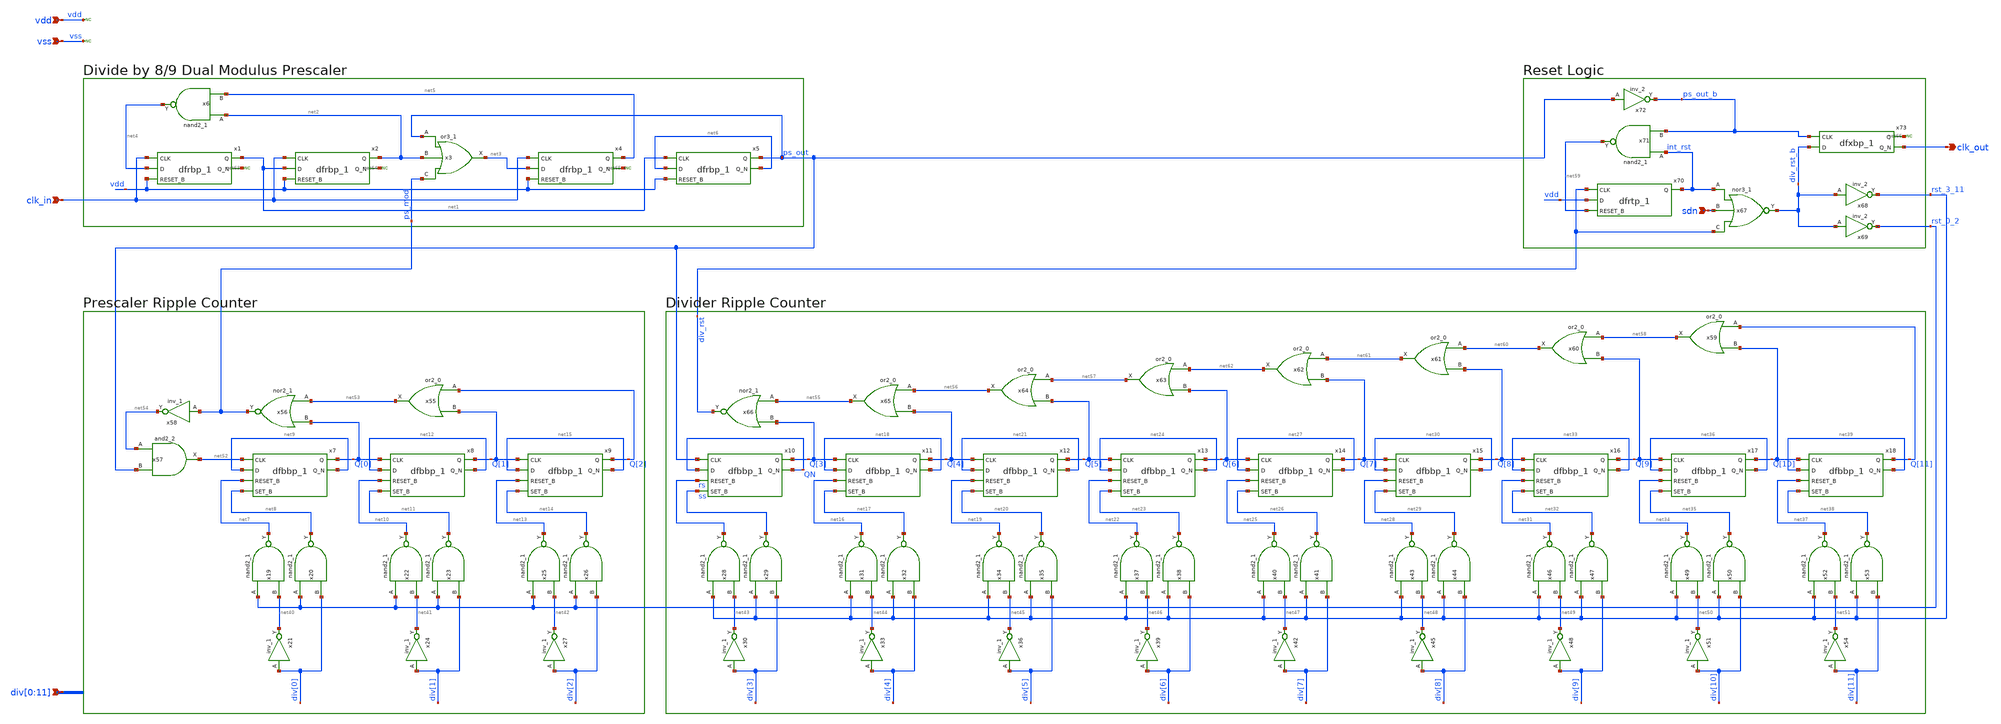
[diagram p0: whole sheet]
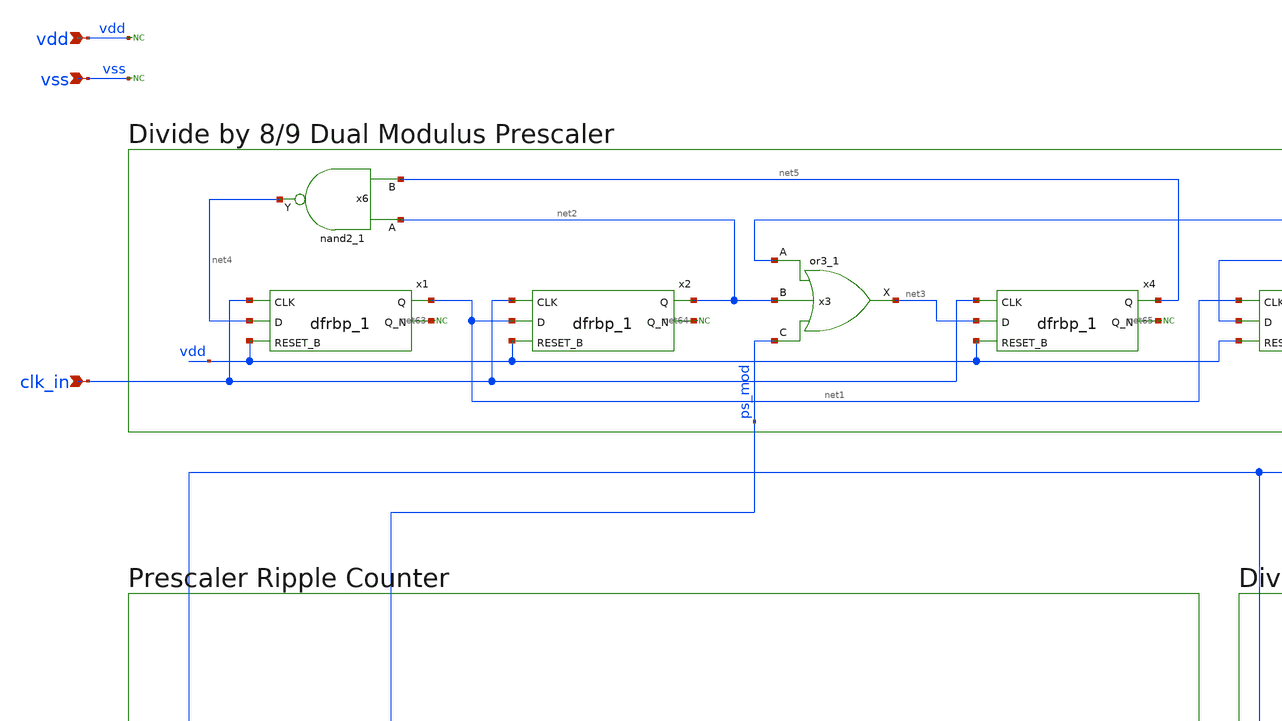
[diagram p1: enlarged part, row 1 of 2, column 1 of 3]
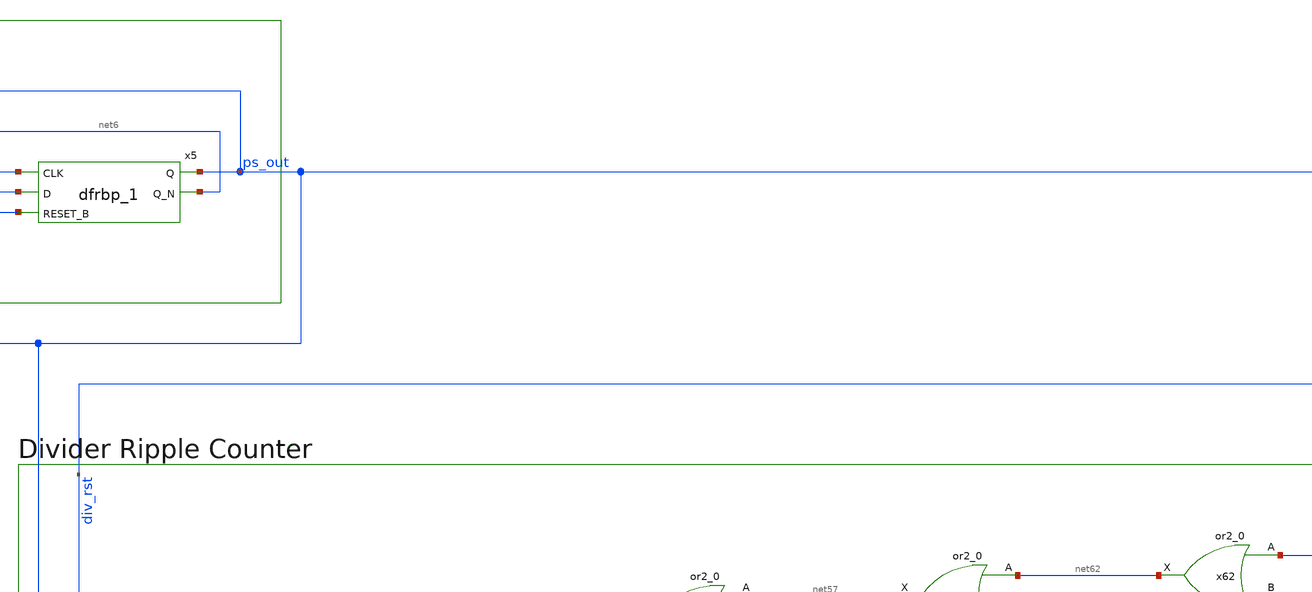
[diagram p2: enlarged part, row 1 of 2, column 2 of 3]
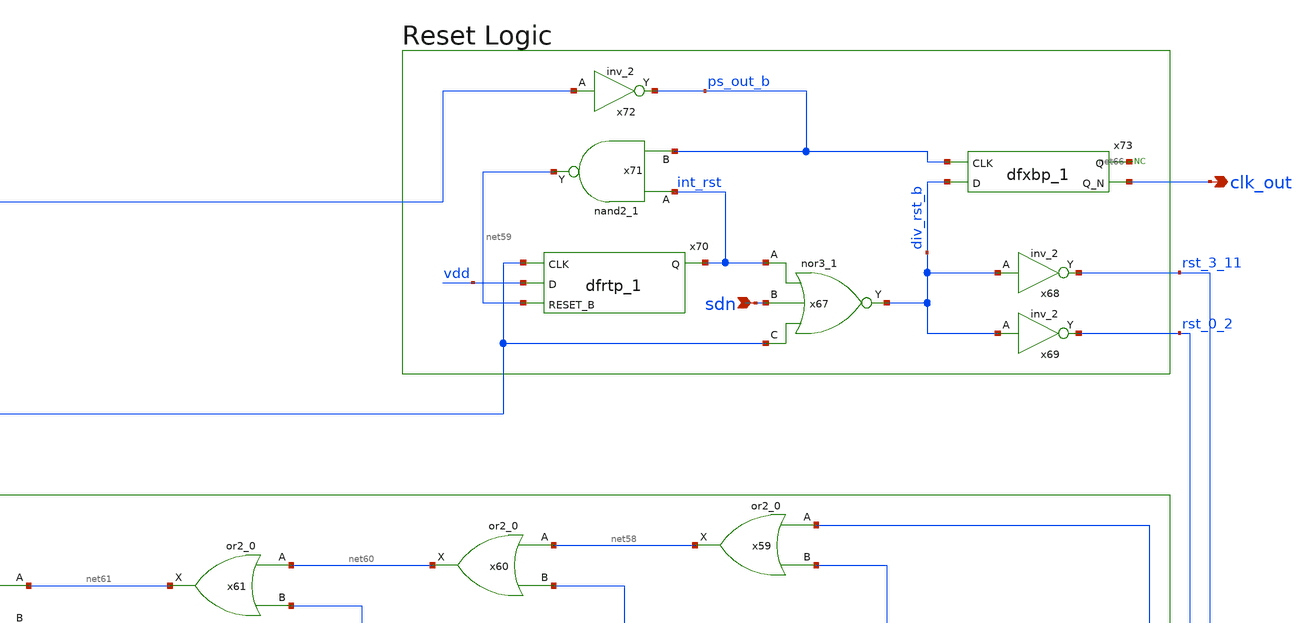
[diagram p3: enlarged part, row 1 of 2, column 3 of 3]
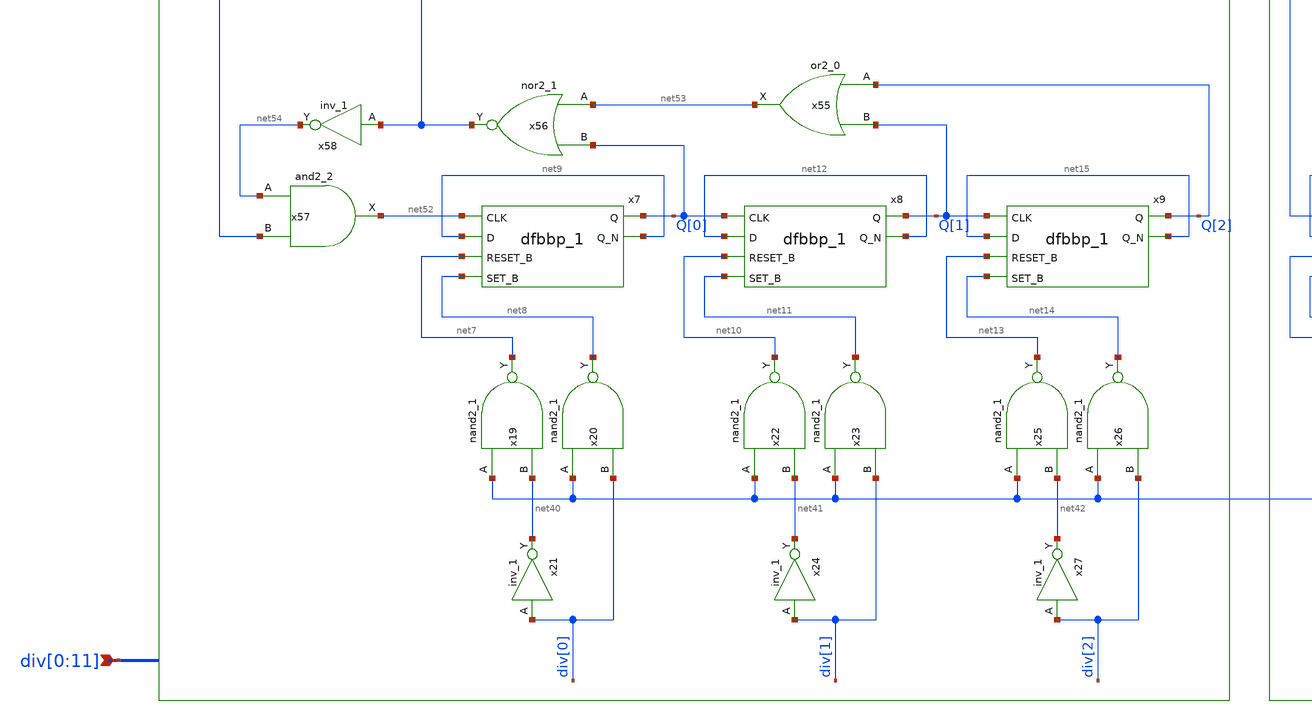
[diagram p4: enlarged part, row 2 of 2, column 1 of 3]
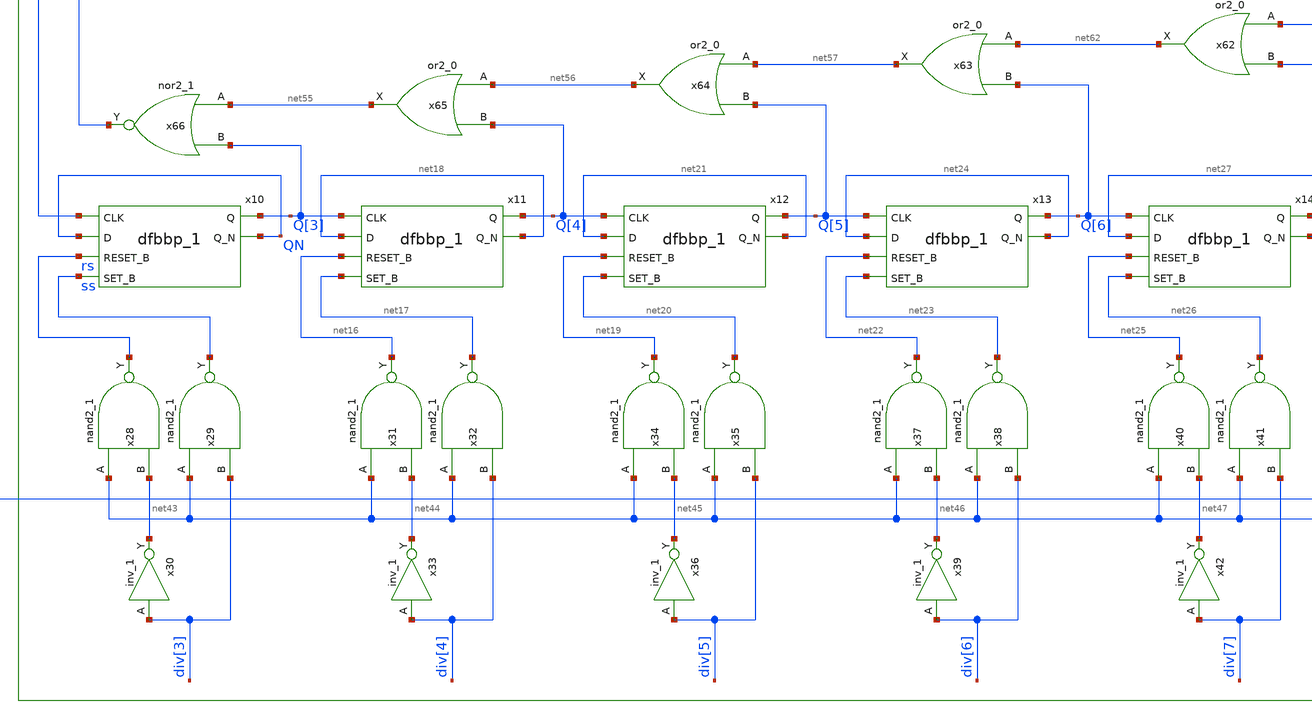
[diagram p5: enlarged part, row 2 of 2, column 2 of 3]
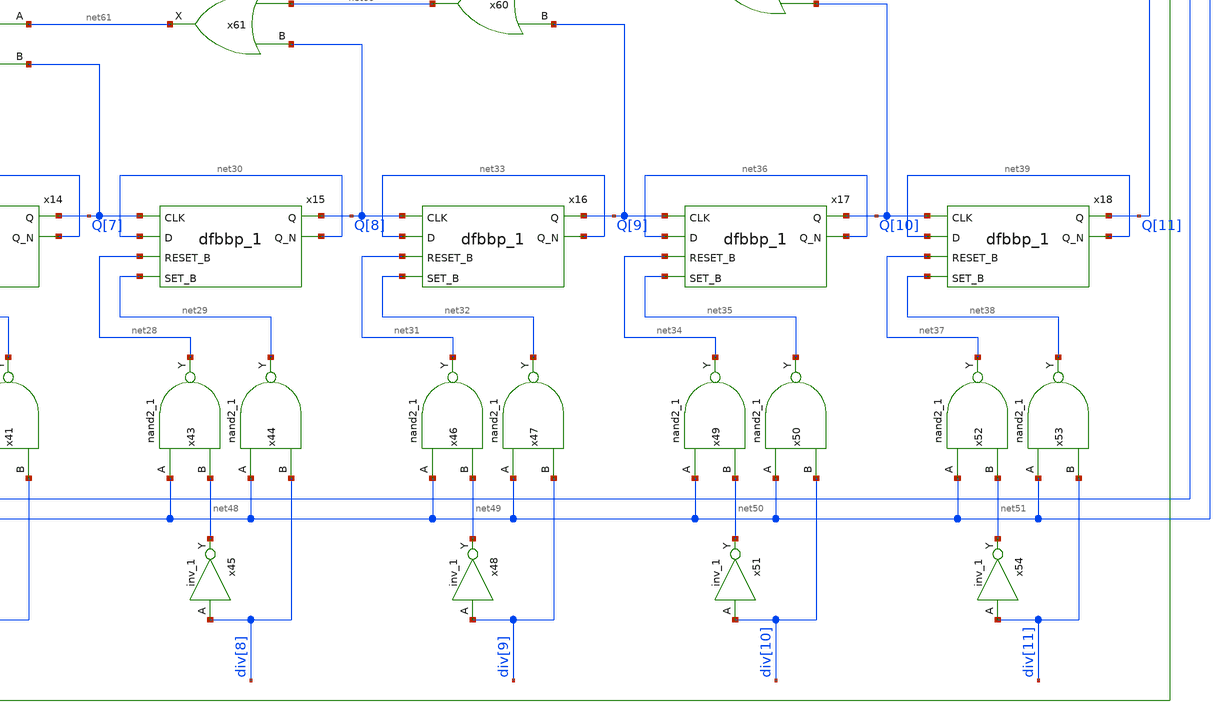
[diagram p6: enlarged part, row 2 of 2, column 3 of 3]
** sch_path: pll/pll_divider/xschem/pll_divider.sch
**.subckt pll_divider clk_in
*+ div[0],div[1],div[2],div[3],div[4],div[5],div[6],div[7],div[8],div[9],div[10],div[11] sdn clk_out vss vdd
*.ipin clk_in
*.ipin div[0],div[1],div[2],div[3],div[4],div[5],div[6],div[7],div[8],div[9],div[10],div[11]
*.ipin sdn
*.opin clk_out
*.ipin vss
*.ipin vdd
x1 clk_in net4 vdd vss vss vdd vdd net1 net63 sky130_fd_sc_hd__dfrbp_1
x2 clk_in net1 vdd vss vss vdd vdd net2 net64 sky130_fd_sc_hd__dfrbp_1
x4 clk_in net3 vdd vss vss vdd vdd net5 net65 sky130_fd_sc_hd__dfrbp_1
x5 net1 net6 vdd vss vss vdd vdd ps_out net6 sky130_fd_sc_hd__dfrbp_1
x3 ps_out net2 ps_mod vss vss vdd vdd net3 sky130_fd_sc_hd__or3_1
x6 net2 net5 vss vss vdd vdd net4 sky130_fd_sc_hd__nand2_1
x7 net52 net9 net7 net8 vss vss vdd vdd Q[0] net9 sky130_fd_sc_hd__dfbbp_1
x8 Q[0] net12 net10 net11 vss vss vdd vdd Q[1] net12 sky130_fd_sc_hd__dfbbp_1
x9 Q[1] net15 net13 net14 vss vss vdd vdd Q[2] net15 sky130_fd_sc_hd__dfbbp_1
x10 ps_out QN rs ss vss vss vdd vdd Q[3] QN sky130_fd_sc_hd__dfbbp_1
x11 Q[3] net18 net16 net17 vss vss vdd vdd Q[4] net18 sky130_fd_sc_hd__dfbbp_1
x12 Q[4] net21 net19 net20 vss vss vdd vdd Q[5] net21 sky130_fd_sc_hd__dfbbp_1
x13 Q[5] net24 net22 net23 vss vss vdd vdd Q[6] net24 sky130_fd_sc_hd__dfbbp_1
x14 Q[6] net27 net25 net26 vss vss vdd vdd Q[7] net27 sky130_fd_sc_hd__dfbbp_1
x15 Q[7] net30 net28 net29 vss vss vdd vdd Q[8] net30 sky130_fd_sc_hd__dfbbp_1
x16 Q[8] net33 net31 net32 vss vss vdd vdd Q[9] net33 sky130_fd_sc_hd__dfbbp_1
x17 Q[9] net36 net34 net35 vss vss vdd vdd Q[10] net36 sky130_fd_sc_hd__dfbbp_1
x18 Q[10] net39 net37 net38 vss vss vdd vdd Q[11] net39 sky130_fd_sc_hd__dfbbp_1
x19 rst_0_2 net40 vss vss vdd vdd net7 sky130_fd_sc_hd__nand2_1
x20 rst_0_2 div[0] vss vss vdd vdd net8 sky130_fd_sc_hd__nand2_1
x21 div[0] vss vss vdd vdd net40 sky130_fd_sc_hd__inv_1
x22 rst_0_2 net41 vss vss vdd vdd net10 sky130_fd_sc_hd__nand2_1
x23 rst_0_2 div[1] vss vss vdd vdd net11 sky130_fd_sc_hd__nand2_1
x24 div[1] vss vss vdd vdd net41 sky130_fd_sc_hd__inv_1
x25 rst_0_2 net42 vss vss vdd vdd net13 sky130_fd_sc_hd__nand2_1
x26 rst_0_2 div[2] vss vss vdd vdd net14 sky130_fd_sc_hd__nand2_1
x27 div[2] vss vss vdd vdd net42 sky130_fd_sc_hd__inv_1
x28 rst_3_11 net43 vss vss vdd vdd rs sky130_fd_sc_hd__nand2_1
x29 rst_3_11 div[3] vss vss vdd vdd ss sky130_fd_sc_hd__nand2_1
x30 div[3] vss vss vdd vdd net43 sky130_fd_sc_hd__inv_1
x31 rst_3_11 net44 vss vss vdd vdd net16 sky130_fd_sc_hd__nand2_1
x32 rst_3_11 div[4] vss vss vdd vdd net17 sky130_fd_sc_hd__nand2_1
x33 div[4] vss vss vdd vdd net44 sky130_fd_sc_hd__inv_1
x34 rst_3_11 net45 vss vss vdd vdd net19 sky130_fd_sc_hd__nand2_1
x35 rst_3_11 div[5] vss vss vdd vdd net20 sky130_fd_sc_hd__nand2_1
x36 div[5] vss vss vdd vdd net45 sky130_fd_sc_hd__inv_1
x37 rst_3_11 net46 vss vss vdd vdd net22 sky130_fd_sc_hd__nand2_1
x38 rst_3_11 div[6] vss vss vdd vdd net23 sky130_fd_sc_hd__nand2_1
x39 div[6] vss vss vdd vdd net46 sky130_fd_sc_hd__inv_1
x40 rst_3_11 net47 vss vss vdd vdd net25 sky130_fd_sc_hd__nand2_1
x41 rst_3_11 div[7] vss vss vdd vdd net26 sky130_fd_sc_hd__nand2_1
x42 div[7] vss vss vdd vdd net47 sky130_fd_sc_hd__inv_1
x43 rst_3_11 net48 vss vss vdd vdd net28 sky130_fd_sc_hd__nand2_1
x44 rst_3_11 div[8] vss vss vdd vdd net29 sky130_fd_sc_hd__nand2_1
x45 div[8] vss vss vdd vdd net48 sky130_fd_sc_hd__inv_1
x46 rst_3_11 net49 vss vss vdd vdd net31 sky130_fd_sc_hd__nand2_1
x47 rst_3_11 div[9] vss vss vdd vdd net32 sky130_fd_sc_hd__nand2_1
x48 div[9] vss vss vdd vdd net49 sky130_fd_sc_hd__inv_1
x49 rst_3_11 net50 vss vss vdd vdd net34 sky130_fd_sc_hd__nand2_1
x50 rst_3_11 div[10] vss vss vdd vdd net35 sky130_fd_sc_hd__nand2_1
x51 div[10] vss vss vdd vdd net50 sky130_fd_sc_hd__inv_1
x52 rst_3_11 net51 vss vss vdd vdd net37 sky130_fd_sc_hd__nand2_1
x53 rst_3_11 div[11] vss vss vdd vdd net38 sky130_fd_sc_hd__nand2_1
x54 div[11] vss vss vdd vdd net51 sky130_fd_sc_hd__inv_1
x55 Q[2] Q[1] vss vss vdd vdd net53 sky130_fd_sc_hd__or2_0
x56 net53 Q[0] vss vss vdd vdd ps_mod sky130_fd_sc_hd__nor2_1
x58 ps_mod vss vss vdd vdd net54 sky130_fd_sc_hd__inv_1
x59 Q[11] Q[10] vss vss vdd vdd net58 sky130_fd_sc_hd__or2_0
x60 net58 Q[9] vss vss vdd vdd net60 sky130_fd_sc_hd__or2_0
x61 net60 Q[8] vss vss vdd vdd net61 sky130_fd_sc_hd__or2_0
x62 net61 Q[7] vss vss vdd vdd net62 sky130_fd_sc_hd__or2_0
x63 net62 Q[6] vss vss vdd vdd net57 sky130_fd_sc_hd__or2_0
x64 net57 Q[5] vss vss vdd vdd net56 sky130_fd_sc_hd__or2_0
x65 net56 Q[4] vss vss vdd vdd net55 sky130_fd_sc_hd__or2_0
x66 net55 Q[3] vss vss vdd vdd div_rst sky130_fd_sc_hd__nor2_1
x67 int_rst sdn div_rst vss vss vdd vdd div_rst_b sky130_fd_sc_hd__nor3_1
x68 div_rst_b vss vss vdd vdd rst_3_11 sky130_fd_sc_hd__inv_2
x69 div_rst_b vss vss vdd vdd rst_0_2 sky130_fd_sc_hd__inv_2
x70 div_rst vdd net59 vss vss vdd vdd int_rst sky130_fd_sc_hd__dfrtp_1
x71 int_rst ps_out_b vss vss vdd vdd net59 sky130_fd_sc_hd__nand2_1
x73 ps_out_b div_rst_b vss vss vdd vdd net66 clk_out sky130_fd_sc_hd__dfxbp_1
x72 ps_out vss vss vdd vdd ps_out_b sky130_fd_sc_hd__inv_2
x57 net54 ps_out vss vss vdd vdd net52 sky130_fd_sc_hd__and2_2
* noconn vss
* noconn vdd
* noconn #net65
* noconn #net64
* noconn #net63
* noconn #net66
**** begin user architecture code

.options wnflag=1
.include $::SKYWATER_MODELS/cells/nfet_01v8/sky130_fd_pr__nfet_01v8__tt.corner.spice
.include $::SKYWATER_MODELS/cells/nfet_01v8_lvt/sky130_fd_pr__nfet_01v8_lvt__tt.corner.spice
.include $::SKYWATER_MODELS/cells/pfet_01v8/sky130_fd_pr__pfet_01v8__tt.corner.spice
.include $::SKYWATER_MODELS/cells/nfet_03v3_nvt/sky130_fd_pr__nfet_03v3_nvt__tt.corner.spice
.include $::SKYWATER_MODELS/cells/nfet_05v0_nvt/sky130_fd_pr__nfet_05v0_nvt__tt.corner.spice
.include $::SKYWATER_MODELS/cells/esd_nfet_01v8/sky130_fd_pr__esd_nfet_01v8__tt.corner.spice
.include $::SKYWATER_MODELS/cells/pfet_01v8_lvt/sky130_fd_pr__pfet_01v8_lvt__tt.corner.spice
.include $::SKYWATER_MODELS/cells/pfet_01v8_hvt/sky130_fd_pr__pfet_01v8_hvt__tt.corner.spice
.include $::SKYWATER_MODELS/cells/esd_pfet_g5v0d10v5/sky130_fd_pr__esd_pfet_g5v0d10v5__tt.corner.spice
.include $::SKYWATER_MODELS/cells/pfet_g5v0d10v5/sky130_fd_pr__pfet_g5v0d10v5__tt.corner.spice
.include $::SKYWATER_MODELS/cells/pfet_g5v0d16v0/sky130_fd_pr__pfet_g5v0d16v0__tt.corner.spice
.include $::SKYWATER_MODELS/cells/nfet_g5v0d10v5/sky130_fd_pr__nfet_g5v0d10v5__tt.corner.spice
.include $::SKYWATER_MODELS/cells/nfet_g5v0d16v0/sky130_fd_pr__nfet_g5v0d16v0__tt_discrete.corner.spice
.include $::SKYWATER_MODELS/cells/esd_nfet_g5v0d10v5/sky130_fd_pr__esd_nfet_g5v0d10v5__tt.corner.spice
.include $::SKYWATER_MODELS/models/corners/tt/nonfet.spice

.include $::SKYWATER_MODELS/cells/cap_var_hvt/sky130_fd_pr__cap_var_hvt.model.spice

* Mismatch parameters
.include $::SKYWATER_MODELS/cells/nfet_01v8/sky130_fd_pr__nfet_01v8__mismatch.corner.spice
.include $::SKYWATER_MODELS/cells/pfet_01v8/sky130_fd_pr__pfet_01v8__mismatch.corner.spice
.include $::SKYWATER_MODELS/cells/nfet_01v8_lvt/sky130_fd_pr__nfet_01v8_lvt__mismatch.corner.spice
.include $::SKYWATER_MODELS/cells/pfet_01v8_lvt/sky130_fd_pr__pfet_01v8_lvt__mismatch.corner.spice
.include $::SKYWATER_MODELS/cells/pfet_01v8_hvt/sky130_fd_pr__pfet_01v8_hvt__mismatch.corner.spice
.include $::SKYWATER_MODELS/cells/nfet_g5v0d10v5/sky130_fd_pr__nfet_g5v0d10v5__mismatch.corner.spice
.include $::SKYWATER_MODELS/cells/pfet_g5v0d10v5/sky130_fd_pr__pfet_g5v0d10v5__mismatch.corner.spice
.include $::SKYWATER_MODELS/cells/nfet_05v0_nvt/sky130_fd_pr__nfet_05v0_nvt__mismatch.corner.spice
.include $::SKYWATER_MODELS/cells/nfet_03v3_nvt/sky130_fd_pr__nfet_03v3_nvt__mismatch.corner.spice

* Resistor$::SKYWATER_MODELS/Capacitor
.include $::SKYWATER_MODELS/models/r+c/res_typical__cap_typical.spice
.include $::SKYWATER_MODELS/models/r+c/res_typical__cap_typical__lin.spice

* Special cells
.include $::SKYWATER_MODELS/models/corners/tt/specialized_cells.spice

* All models
.include $::SKYWATER_MODELS/models/all.spice

* Corner
.include $::SKYWATER_MODELS/models/corners/tt/rf.spice

* .include $::SKYWATER_STDCELLS/cells/
.include $::SKYWATER_STDCELLS/cells/buf/sky130_fd_sc_hd__buf_1.spice
.include $::SKYWATER_STDCELLS_HS/cells/buf/sky130_fd_sc_hs__buf_1.spice
.include $::SKYWATER_STDCELLS_HS/cells/buf/sky130_fd_sc_hs__buf_16.spice
.include $::SKYWATER_STDCELLS/cells/clkbuf/sky130_fd_sc_hd__clkbuf_1.spice
.include $::SKYWATER_STDCELLS/cells/clkbuf/sky130_fd_sc_hd__clkbuf_2.spice
.include $::SKYWATER_STDCELLS/cells/clkbuf/sky130_fd_sc_hd__clkbuf_4.spice
.include $::SKYWATER_STDCELLS/cells/clkbuf/sky130_fd_sc_hd__clkbuf_8.spice
.include $::SKYWATER_STDCELLS/cells/clkbuf/sky130_fd_sc_hd__clkbuf_16.spice
.include $::SKYWATER_STDCELLS/cells/decap/sky130_fd_sc_hd__decap_3.spice
.include $::SKYWATER_STDCELLS/cells/decap/sky130_fd_sc_hd__decap_4.spice
.include $::SKYWATER_STDCELLS/cells/decap/sky130_fd_sc_hd__decap_8.spice
.include $::SKYWATER_STDCELLS/cells/dfrbp/sky130_fd_sc_hd__dfrbp_1.spice
.include $::SKYWATER_STDCELLS/cells/dfrbp/sky130_fd_sc_hd__dfrbp_2.spice
.include $::SKYWATER_STDCELLS/cells/inv/sky130_fd_sc_hd__inv_1.spice
.include $::SKYWATER_STDCELLS/cells/inv/sky130_fd_sc_hd__inv_2.spice
.include $::SKYWATER_STDCELLS/cells/inv/sky130_fd_sc_hd__inv_4.spice
.include $::SKYWATER_STDCELLS/cells/inv/sky130_fd_sc_hd__inv_8.spice
.include $::SKYWATER_STDCELLS/cells/inv/sky130_fd_sc_hd__inv_16.spice
.include $::SKYWATER_STDCELLS_HS/cells/inv/sky130_fd_sc_hs__inv_1.spice
.include $::SKYWATER_STDCELLS_HS/cells/inv/sky130_fd_sc_hs__inv_2.spice
.include $::SKYWATER_STDCELLS_HS/cells/inv/sky130_fd_sc_hs__inv_4.spice
.include $::SKYWATER_STDCELLS_HS/cells/inv/sky130_fd_sc_hs__inv_8.spice
.include $::SKYWATER_STDCELLS_HS/cells/inv/sky130_fd_sc_hs__inv_16.spice
.include $::SKYWATER_STDCELLS/cells/mux2/sky130_fd_sc_hd__mux2_2.spice
.include $::SKYWATER_STDCELLS/cells/and2/sky130_fd_sc_hd__and2_1.spice
.include $::SKYWATER_STDCELLS/cells/and2/sky130_fd_sc_hd__and2_2.spice
.include $::SKYWATER_STDCELLS/cells/nand2/sky130_fd_sc_hd__nand2_1.spice
.include $::SKYWATER_STDCELLS/cells/tap/sky130_fd_sc_hd__tap_2.spice
.include $::SKYWATER_STDCELLS/cells/tapvpwrvgnd/sky130_fd_sc_hd__tapvpwrvgnd_1.spice
.include $::SKYWATER_STDCELLS/cells/dfbbn/sky130_fd_sc_hd__dfbbn_1.spice
.include $::SKYWATER_STDCELLS/cells/dfbbn/sky130_fd_sc_hd__dfbbn_2.spice
.include $::SKYWATER_STDCELLS/cells/dfbbp/sky130_fd_sc_hd__dfbbp_1.spice
.include $::SKYWATER_STDCELLS_HS/cells/dfbbn/sky130_fd_sc_hs__dfbbn_1.spice
.include $::SKYWATER_STDCELLS_HS/cells/dfbbn/sky130_fd_sc_hs__dfbbn_2.spice
.include $::SKYWATER_STDCELLS_HS/cells/dfrbp/sky130_fd_sc_hs__dfrbp_1.spice
.include $::SKYWATER_STDCELLS_HS/cells/dfrbp/sky130_fd_sc_hs__dfrbp_2.spice
.include $::SKYWATER_STDCELLS/cells/dfrtp/sky130_fd_sc_hd__dfrtp_1.spice
.include $::SKYWATER_STDCELLS/cells/dfrtp/sky130_fd_sc_hd__dfrtp_2.spice
.include $::SKYWATER_STDCELLS/cells/dfxbp/sky130_fd_sc_hd__dfxbp_1.spice
.include $::SKYWATER_STDCELLS/cells/dfxbp/sky130_fd_sc_hd__dfxbp_2.spice
.include $::SKYWATER_STDCELLS/cells/or2/sky130_fd_sc_hd__or2_0.spice
.include $::SKYWATER_STDCELLS/cells/or3/sky130_fd_sc_hd__or3_1.spice
.include $::SKYWATER_STDCELLS/cells/nor2/sky130_fd_sc_hd__nor2_1.spice
.include $::SKYWATER_STDCELLS/cells/nor3/sky130_fd_sc_hd__nor3_1.spice

**** end user architecture code
**.ends
.end
